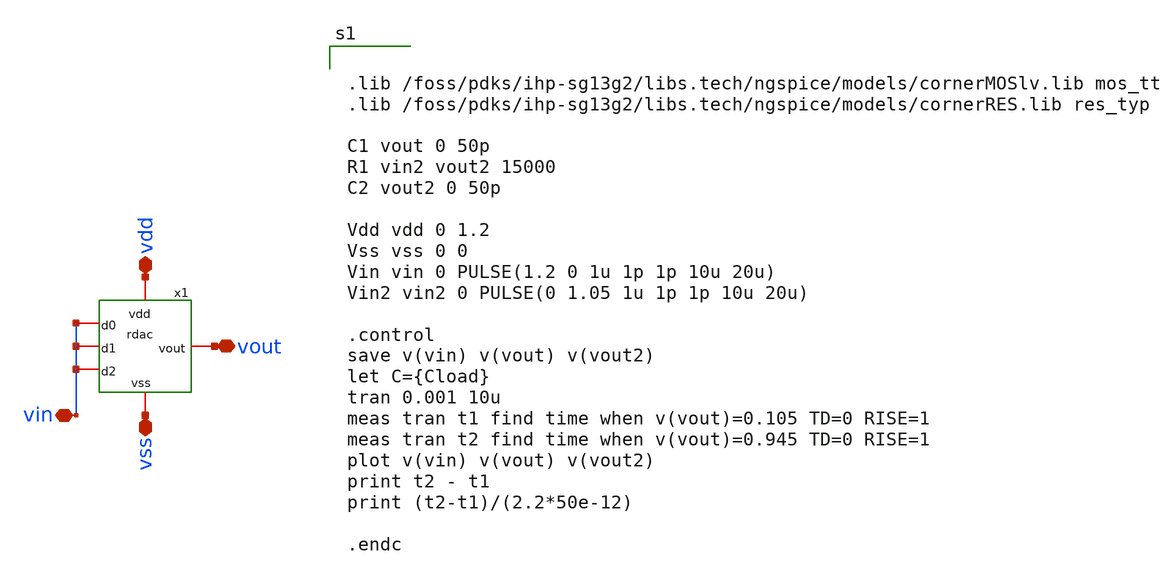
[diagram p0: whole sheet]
** sch_path: xschem/rdac_tb_tran.sch
**.subckt rdac_tb_tran vout vss vin vdd
*.iopin vout
*.iopin vss
*.iopin vin
*.iopin vdd
x1 vdd vin vout vin vin vss rdac
**** begin user architecture code


.lib /foss/pdks/ihp-sg13g2/libs.tech/ngspice/models/cornerMOSlv.lib mos_tt
.lib /foss/pdks/ihp-sg13g2/libs.tech/ngspice/models/cornerRES.lib res_typ

C1 vout 0 50p
R1 vin2 vout2 15000
C2 vout2 0 50p

Vdd vdd 0 1.2
Vss vss 0 0
Vin vin 0 PULSE(1.2 0 1u 1p 1p 10u 20u)
Vin2 vin2 0 PULSE(0 1.05 1u 1p 1p 10u 20u)

.control
save v(vin) v(vout) v(vout2)
let C={Cload}
tran 0.001 10u
meas tran t1 find time when v(vout)=0.105 TD=0 RISE=1
meas tran t2 find time when v(vout)=0.945 TD=0 RISE=1
plot v(vin) v(vout) v(vout2)
print t2 - t1
print (t2-t1)/(2.2*50e-12)

.endc


**** end user architecture code
**.ends

* expanding   symbol:  rdac.sym # of pins=6
** sym_path: xschem/rdac.sym
** sch_path: xschem/rdac.sch
.subckt rdac vdd d0 vout d1 d2 vss
*.iopin vout
*.iopin vdd
*.iopin d0
*.iopin vss
*.iopin d1
*.iopin d2
x1 vdd d0 net5 vss inverter
x2 vdd d1 net4 vss inverter
x3 vdd d2 net1 vss inverter
XR1 net1 vout sub! rhigh w=0.5e-6 l=10.0e-6 m=1 b=0 mm_ok=1
XR2 net4 net2 sub! rhigh w=0.5e-6 l=10.0e-6 m=1 b=0 mm_ok=1
XR3 net5 net3 sub! rhigh w=0.5e-6 l=10.0e-6 m=1 b=0 mm_ok=1
XR4 vss net3 sub! rhigh w=0.5e-6 l=10.0e-6 m=1 b=0 mm_ok=1
XR5 vout net2 sub! rhigh w=0.5e-6 l=5.0e-6 m=1 b=0 mm_ok=1
XR6 net2 net3 sub! rhigh w=0.5e-6 l=5.0e-6 m=1 b=0 mm_ok=1
.ends


* expanding   symbol:  inverter.sym # of pins=4
** sym_path: xschem/inverter.sym
** sch_path: xschem/inverter.sch
.subckt inverter vdd vin vout vss
*.iopin vout
*.iopin vss
*.iopin vin
*.iopin vdd
XM1 vout vin vss vss sg13_lv_nmos w=1.5u l=0.13u ng=1 m=1 mm_ok=1
XM2 vout vin vdd vdd sg13_lv_pmos w=3.0u l=0.13u ng=1 m=1 mm_ok=1
.ends

.end
